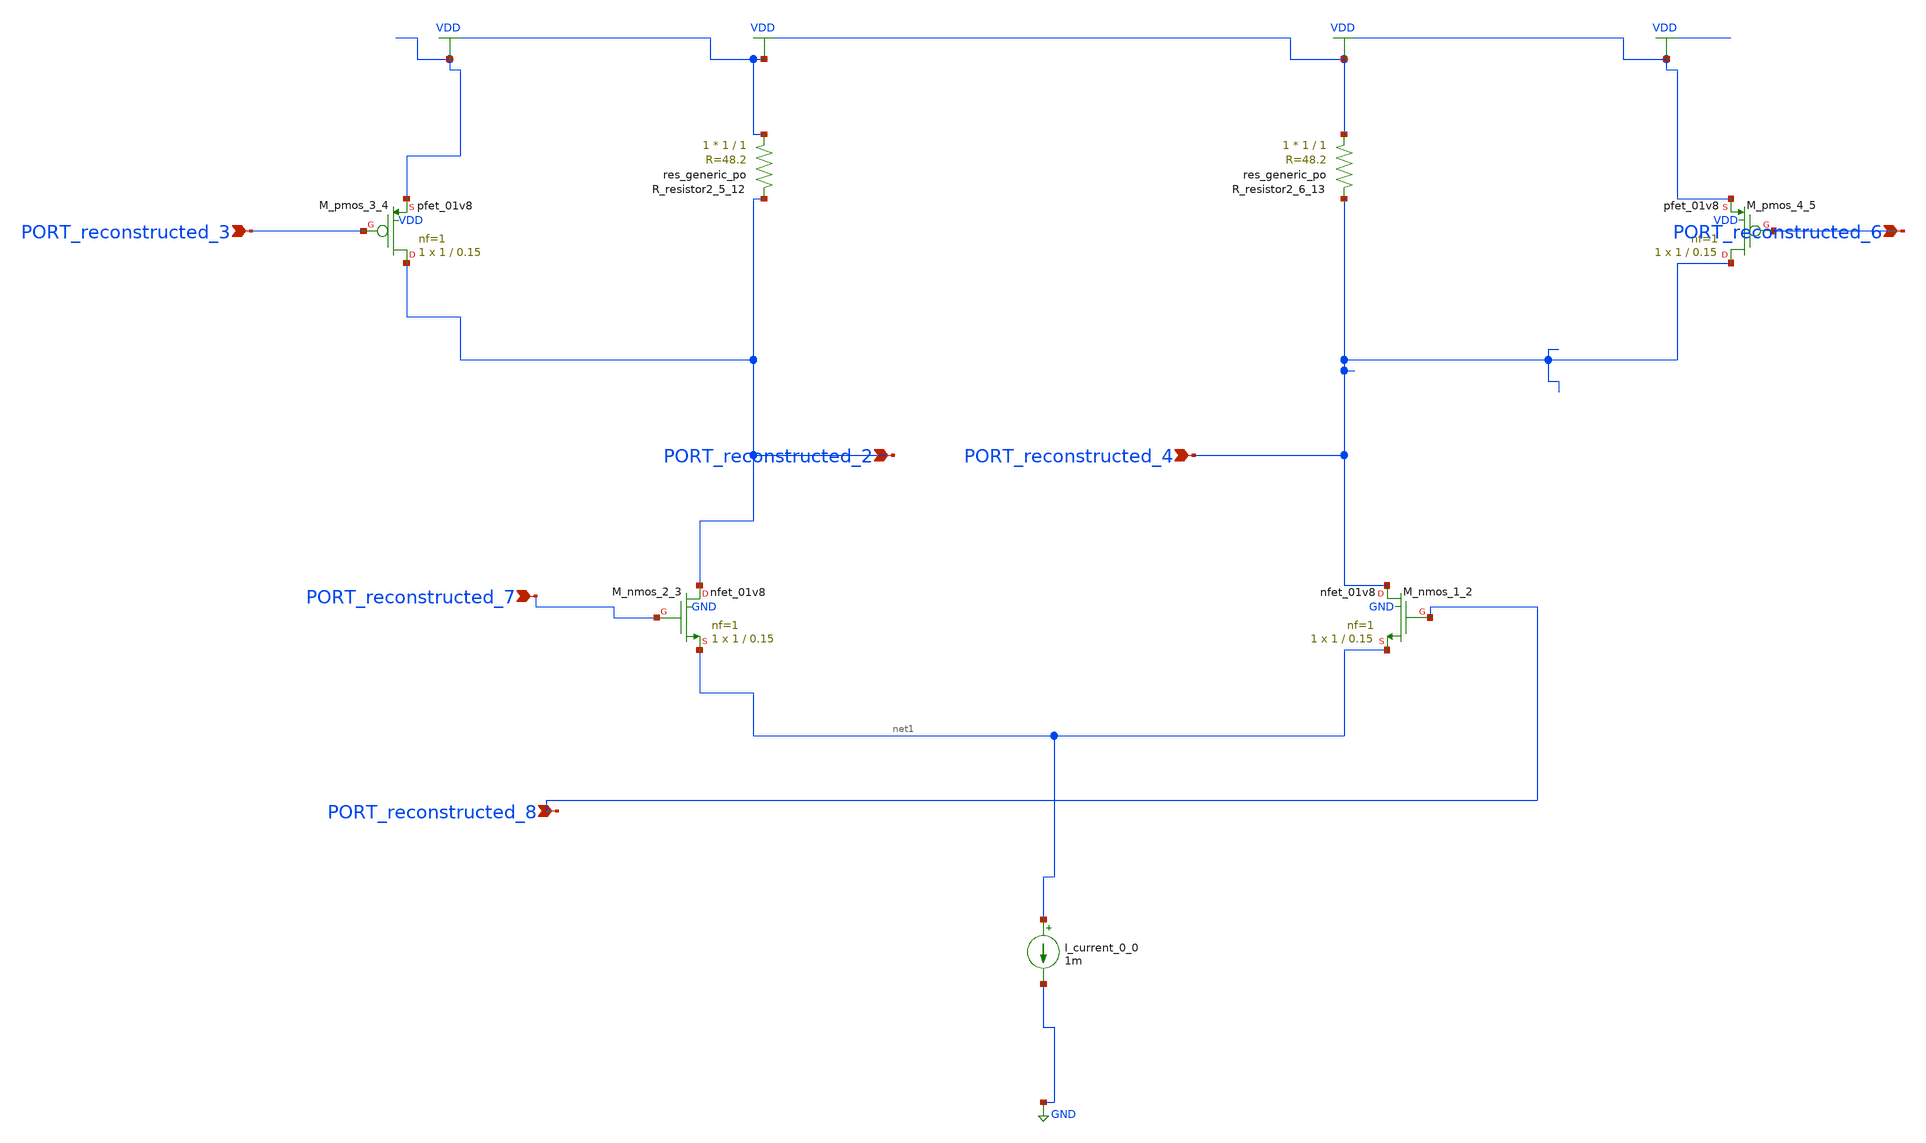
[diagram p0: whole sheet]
** sch_path: schematics/AMSNet/225.sch
**.subckt 225 PORT_reconstructed_3 PORT_reconstructed_7 PORT_reconstructed_8 PORT_reconstructed_6
*+ PORT_reconstructed_4 PORT_reconstructed_2
*.ipin PORT_reconstructed_3
*.ipin PORT_reconstructed_7
*.ipin PORT_reconstructed_8
*.ipin PORT_reconstructed_6
*.ipin PORT_reconstructed_4
*.ipin PORT_reconstructed_2
I_current_0_0 net1 GND 1m
XM_nmos_1_2 PORT_reconstructed_4 PORT_reconstructed_8 net1 GND sky130_fd_pr__nfet_01v8 L=0.15 W=1 nf=1
+ ad='int((1 + 1)/2) * 1 / 1 * 0.29' as='int((1 + 2)/2) * 1 / 1 * 0.29' pd='2*int((1 + 1)/2) * (1 / 1 + 0.29)'
+ ps='2*int((1 + 2)/2) * (1 / 1 + 0.29)' nrd='0.29 / 1 ' nrs='0.29 / 1 ' sa=0 sb=0 sd=0 mult=1 m=1
XM_nmos_2_3 PORT_reconstructed_2 PORT_reconstructed_7 net1 GND sky130_fd_pr__nfet_01v8 L=0.15 W=1 nf=1
+ ad='int((1 + 1)/2) * 1 / 1 * 0.29' as='int((1 + 2)/2) * 1 / 1 * 0.29' pd='2*int((1 + 1)/2) * (1 / 1 + 0.29)'
+ ps='2*int((1 + 2)/2) * (1 / 1 + 0.29)' nrd='0.29 / 1 ' nrs='0.29 / 1 ' sa=0 sb=0 sd=0 mult=1 m=1
XM_pmos_3_4 PORT_reconstructed_2 PORT_reconstructed_3 VDD VDD sky130_fd_pr__pfet_01v8 L=0.15 W=1 nf=1
+ ad='int((1 + 1)/2) * 1 / 1 * 0.29' as='int((1 + 2)/2) * 1 / 1 * 0.29' pd='2*int((1 + 1)/2) * (1 / 1 + 0.29)'
+ ps='2*int((1 + 2)/2) * (1 / 1 + 0.29)' nrd='0.29 / 1 ' nrs='0.29 / 1 ' sa=0 sb=0 sd=0 mult=1 m=1
XM_pmos_4_5 PORT_reconstructed_4 PORT_reconstructed_6 VDD VDD sky130_fd_pr__pfet_01v8 L=0.15 W=1 nf=1
+ ad='int((1 + 1)/2) * 1 / 1 * 0.29' as='int((1 + 2)/2) * 1 / 1 * 0.29' pd='2*int((1 + 1)/2) * (1 / 1 + 0.29)'
+ ps='2*int((1 + 2)/2) * (1 / 1 + 0.29)' nrd='0.29 / 1 ' nrs='0.29 / 1 ' sa=0 sb=0 sd=0 mult=1 m=1
XR_resistor2_5_12 VDD PORT_reconstructed_2 sky130_fd_pr__res_generic_po W=1 L=1 m=1
XR_resistor2_6_13 VDD PORT_reconstructed_4 sky130_fd_pr__res_generic_po W=1 L=1 m=1
**.ends
.GLOBAL GND
.GLOBAL VDD
.end
